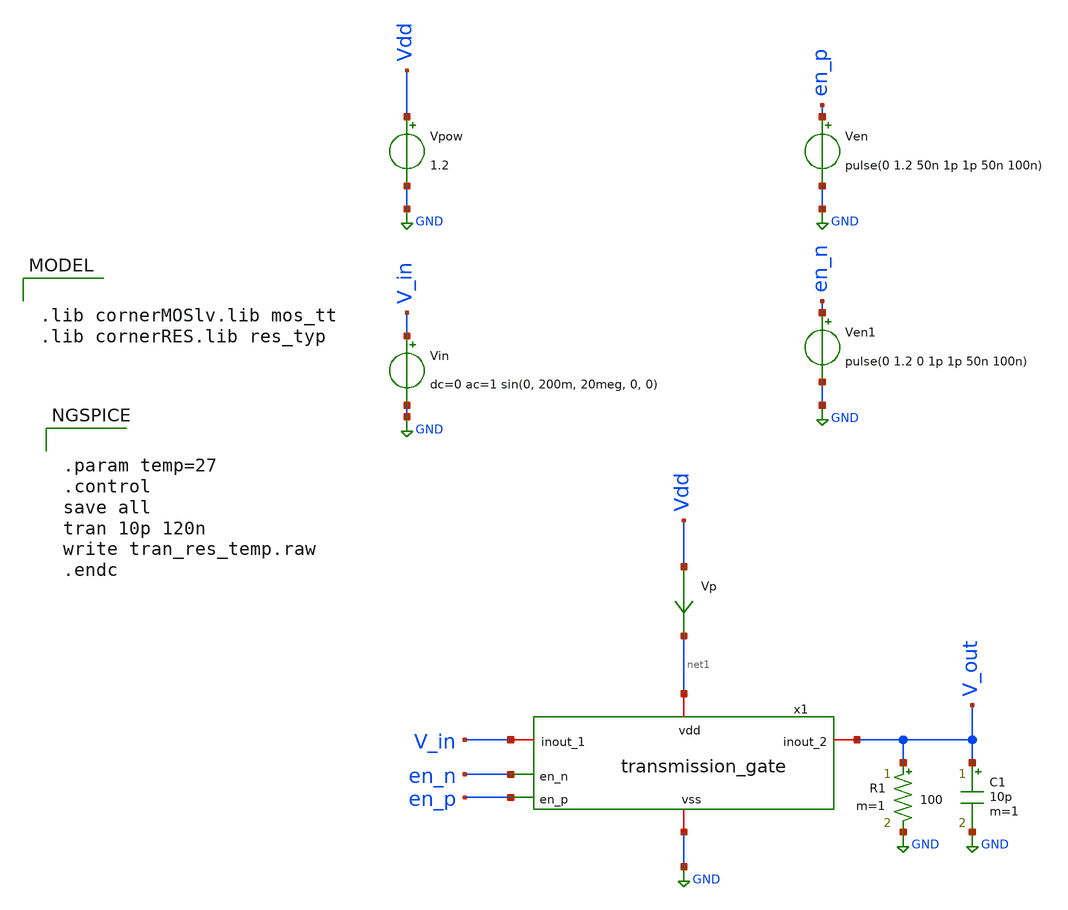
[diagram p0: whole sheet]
** sch_path: CHIPCHILE_CANELOS24_WorkshopTO/design_data/xschem/tgate/transmission_gate_tb.sch
* Copyright 2023 IHP PDK Authors
**.subckt transmission_gate_tb
Vpow Vdd GND 1.2
Vp Vdd net1 0
.save i(vp)
Vin V_in GND dc=0 ac=1 sin(0, 200m, 20meg, 0, 0)
Ven en_p GND pulse(0 1.2 50n 1p 1p 50n 100n)
C1 V_out GND 10p m=1
Ven1 en_n GND pulse(0 1.2 0 1p 1p 50n 100n)
x1 net1 en_n V_in V_out en_p GND transmission_gate
R1 V_out GND 100 m=1
**** begin user architecture code

.lib cornerMOSlv.lib mos_tt
.lib cornerRES.lib res_typ



.param temp=27
.control
save all
tran 10p 120n
write tran_res_temp.raw
.endc


**** end user architecture code
**.ends

* expanding   symbol:  transmission_gate.sym # of pins=6
** sym_path: CHIPCHILE_CANELOS24_WorkshopTO/design_data/xschem/multiplexer/transmission_gate.sym
** sch_path: CHIPCHILE_CANELOS24_WorkshopTO/design_data/xschem/multiplexer/transmission_gate.sch
.subckt transmission_gate vdd en_n inout_1 inout_2 en_p vss
*.iopin inout_1
*.iopin inout_2
*.ipin en_p
*.iopin vdd
*.iopin vss
*.ipin en_n
XM1 inout_1 en_p inout_2 net1 sg13_lv_nmos w=200.0u l=0.130u ng=20 m=1 mm_ok=1
XM2 inout_1 en_n inout_2 net2 sg13_lv_pmos w=200.0u l=0.130u ng=20 m=1 mm_ok=1
XR1 vdd net2 ntap1 R=262.8 w=0.78e-6 l=0.78e-6
XR2 vss net1 ptap1 R=262.8 w=0.78e-6 l=0.78e-6
.ends

.GLOBAL GND
.end
